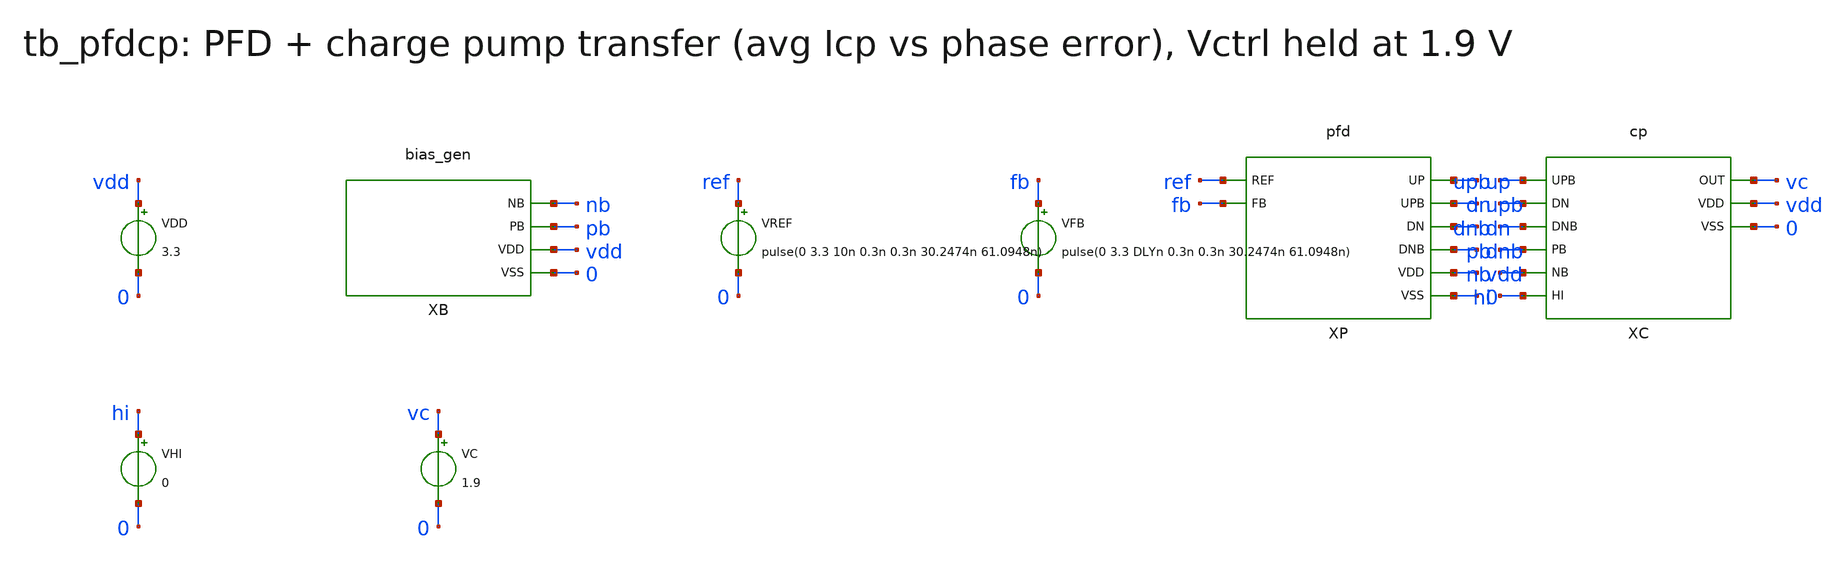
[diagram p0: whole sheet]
** sch_path: v1_claude/xschem/tb_pfdcp.sch
**.subckt tb_pfdcp
VDD vdd 0 3.3
XB nb pb vdd 0 bias_gen
VREF ref 0 pulse(0 3.3 10n 0.3n 0.3n 30.2474n 61.0948n)
VFB fb 0 pulse(0 3.3 DLYn 0.3n 0.3n 30.2474n 61.0948n)
XP ref fb up upb dn dnb vdd 0 pfd
XC upb dn dnb pb nb hi vc vdd 0 cp
VHI hi 0 0
VC vc 0 1.9
**** begin user architecture code
 .include $::180MCU_MODELS/design.ngspice
.lib $::180MCU_MODELS/sm141064.ngspice typical
.lib $::180MCU_MODELS/sm141064.ngspice res_typical
.lib $::180MCU_MODELS/sm141064.ngspice mimcap_typical

.option method=gear
.control
set num_threads=1
tran 10p 400n
meas tran q integ i(VC) from=132.1896n to=376.5689n
let iavg = -q/(244.3793n)
meas tran upw when v(up)=1.65 rise=8
meas tran upf when v(up)=1.65 fall=8
echo RES dly=DLY iavg=$&iavg
.endc

**** end user architecture code
**.ends
.end
